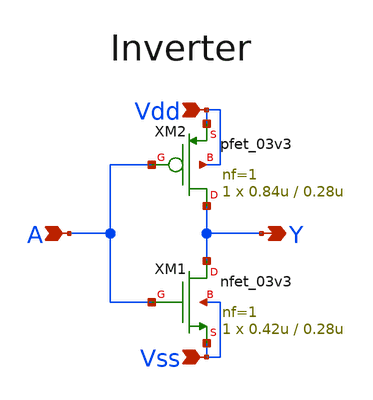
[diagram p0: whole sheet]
** sch_path: designs/libs/core_digital/schem/inv1.sch
**.subckt inv1 Vdd A Vss Y
*.ipin Vdd
*.ipin A
*.ipin Vss
*.opin Y
XM1 Y A Vss Vss nfet_03v3 L=0.28u W=0.42u nf=1 ad='int((nf+1)/2) * W/nf * 0.18u' as='int((nf+2)/2) * W/nf * 0.18u'
+ pd='2*int((nf+1)/2) * (W/nf + 0.18u)' ps='2*int((nf+2)/2) * (W/nf + 0.18u)' nrd='0.18u / W' nrs='0.18u / W'
+ sa=0 sb=0 sd=0 m=1
XM2 Y A Vdd Vdd pfet_03v3 L=0.28u W=0.84u nf=1 ad='int((nf+1)/2) * W/nf * 0.18u' as='int((nf+2)/2) * W/nf * 0.18u'
+ pd='2*int((nf+1)/2) * (W/nf + 0.18u)' ps='2*int((nf+2)/2) * (W/nf + 0.18u)' nrd='0.18u / W' nrs='0.18u / W'
+ sa=0 sb=0 sd=0 m=1
**.ends
.end
